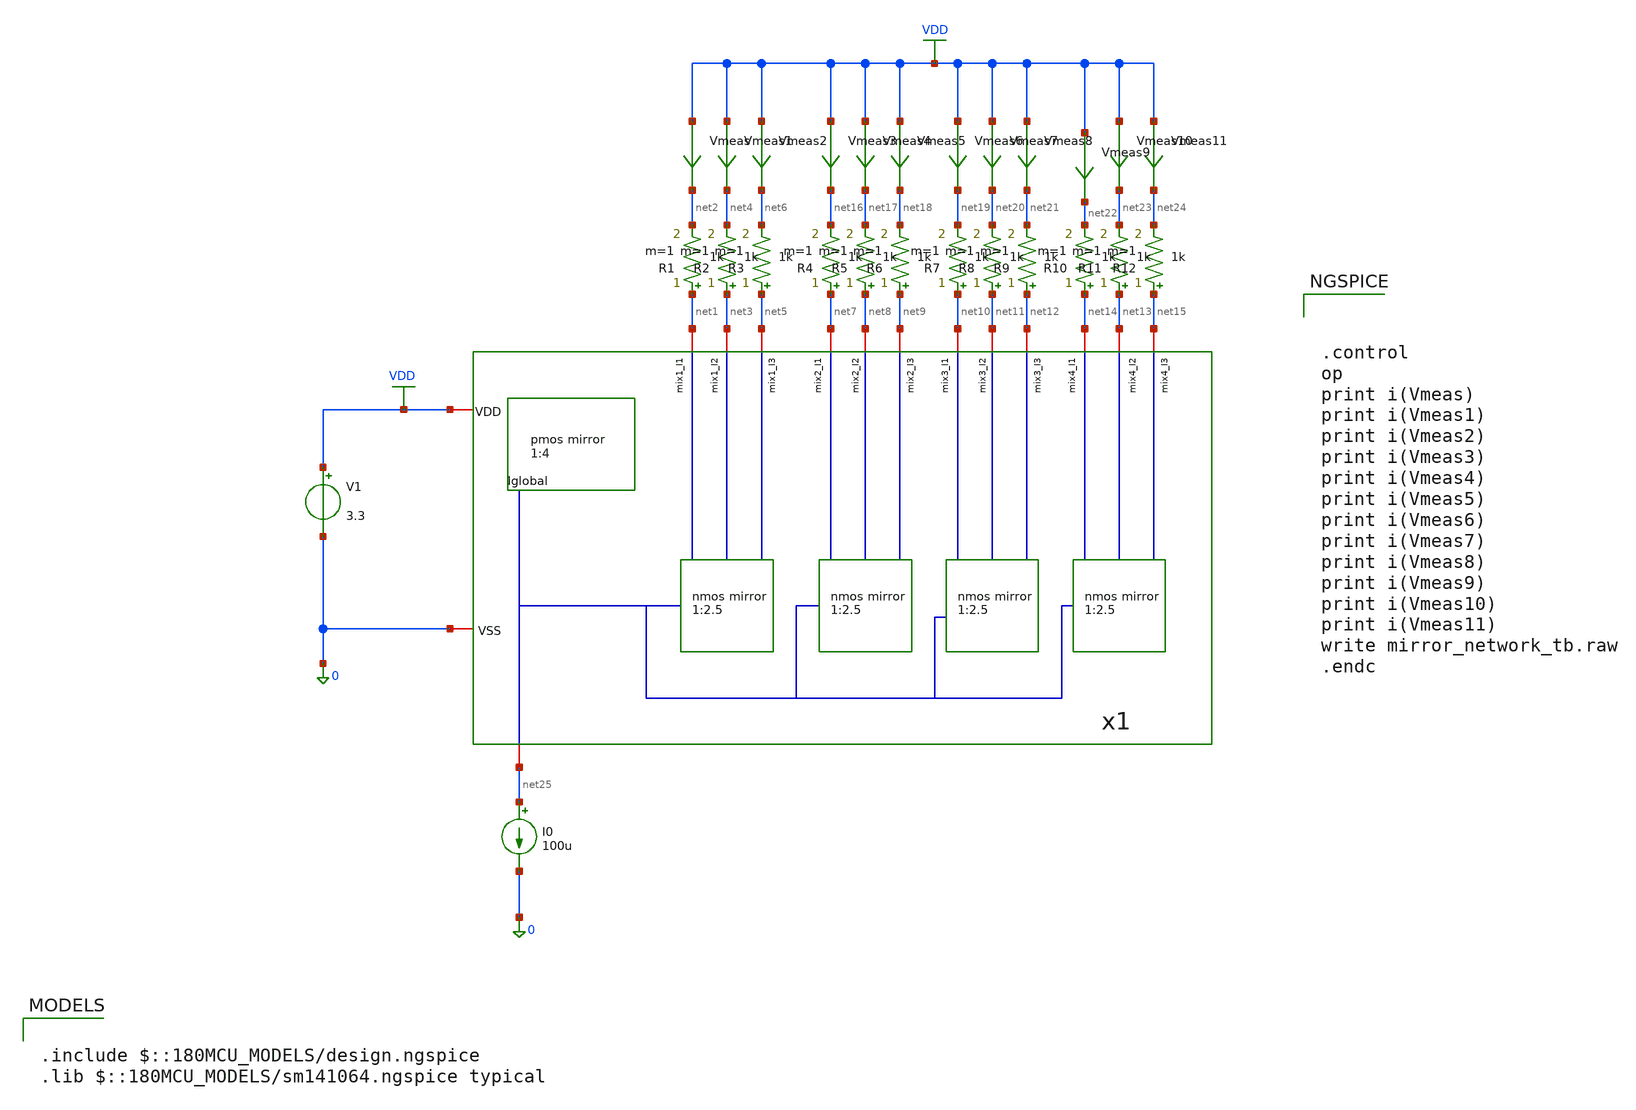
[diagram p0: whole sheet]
** sch_path: designs/mirrors/testbench/mirror_network_tb.sch
**.subckt mirror_network_tb
x1 VDD net25 net14 net1 net13 net15 net3 net5 0 net10 net11 net12 net7 net8 net9 mirror_network
V1 VDD 0 3.3
I0 net25 0 100u
R1 net1 net2 1k m=1
R2 net3 net4 1k m=1
R3 net5 net6 1k m=1
R4 net7 net16 1k m=1
R5 net8 net17 1k m=1
R6 net9 net18 1k m=1
R7 net10 net19 1k m=1
R8 net11 net20 1k m=1
R9 net12 net21 1k m=1
R10 net14 net22 1k m=1
R11 net13 net23 1k m=1
R12 net15 net24 1k m=1
Vmeas VDD net2 0
.save i(vmeas)
Vmeas1 VDD net4 0
.save i(vmeas1)
Vmeas2 VDD net6 0
.save i(vmeas2)
Vmeas3 VDD net16 0
.save i(vmeas3)
Vmeas4 VDD net17 0
.save i(vmeas4)
Vmeas5 VDD net18 0
.save i(vmeas5)
Vmeas6 VDD net19 0
.save i(vmeas6)
Vmeas7 VDD net20 0
.save i(vmeas7)
Vmeas8 VDD net21 0
.save i(vmeas8)
Vmeas9 VDD net22 0
.save i(vmeas9)
Vmeas10 VDD net23 0
.save i(vmeas10)
Vmeas11 VDD net24 0
.save i(vmeas11)
**** begin user architecture code

.include $::180MCU_MODELS/design.ngspice
.lib $::180MCU_MODELS/sm141064.ngspice typical




.control
op
print i(Vmeas)
print i(Vmeas1)
print i(Vmeas2)
print i(Vmeas3)
print i(Vmeas4)
print i(Vmeas5)
print i(Vmeas6)
print i(Vmeas7)
print i(Vmeas8)
print i(Vmeas9)
print i(Vmeas10)
print i(Vmeas11)
write mirror_network_tb.raw
.endc


**** end user architecture code
**.ends

* expanding   symbol:  /foss/designs/NYCMOS/designs/mirrors/schematic/mirror_network.sym # of
*+ pins=15
** sym_path: designs/mirrors/schematic/mirror_network.sym
** sch_path: designs/mirrors/schematic/mirror_network.sch
.subckt mirror_network VDD Iglobal mix4_I1 mix1_I1 mix4_I2 mix4_I3 mix1_I2 mix1_I3 VSS mix3_I1
+ mix3_I2 mix3_I3 mix2_I1 mix2_I2 mix2_I3
*.iopin VSS
*.iopin VDD
*.iopin Iglobal
*.iopin mix1_I1
*.iopin mix1_I2
*.iopin mix1_I3
*.iopin mix2_I1
*.iopin mix2_I2
*.iopin mix2_I3
*.iopin mix3_I1
*.iopin mix3_I2
*.iopin mix3_I3
*.iopin mix4_I1
*.iopin mix4_I2
*.iopin mix4_I3
x1 VDD net1 Iglobal pmos_mirror
x2 net1 mix1_I1 mix1_I2 mix1_I3 VSS nmos_mirror
x3 net1 mix2_I1 mix2_I2 mix2_I3 VSS nmos_mirror
x4 net1 mix3_I1 mix3_I2 mix3_I3 VSS nmos_mirror
x5 net1 mix4_I1 mix4_I2 mix4_I3 VSS nmos_mirror
.ends


* expanding   symbol:  /foss/designs/NYCMOS/designs/mirrors/schematic/pmos_mirror.sym # of pins=3
** sym_path: designs/mirrors/schematic/pmos_mirror.sym
** sch_path: designs/mirrors/schematic/pmos_mirror.sch
.subckt pmos_mirror VDD Iout Iref
*.iopin Iref
*.iopin Iout
*.iopin VDD
XM1 Iref Iref VDD VDD pfet_03v3 L=0.5u W=28u nf=7 ad='int((nf+1)/2) * W/nf * 0.18u' as='int((nf+2)/2) * W/nf * 0.18u'
+ pd='2*int((nf+1)/2) * (W/nf + 0.18u)' ps='2*int((nf+2)/2) * (W/nf + 0.18u)' nrd='0.18u / W' nrs='0.18u / W'
+ sa=0 sb=0 sd=0 m=1
XM2 Iout Iref VDD VDD pfet_03v3 L=0.5u W=28u nf=7 ad='int((nf+1)/2) * W/nf * 0.18u' as='int((nf+2)/2) * W/nf * 0.18u'
+ pd='2*int((nf+1)/2) * (W/nf + 0.18u)' ps='2*int((nf+2)/2) * (W/nf + 0.18u)' nrd='0.18u / W' nrs='0.18u / W'
+ sa=0 sb=0 sd=0 m=1
.ends


* expanding   symbol:  /foss/designs/NYCMOS/designs/mirrors/schematic/nmos_mirror.sym # of pins=5
** sym_path: designs/mirrors/schematic/nmos_mirror.sym
** sch_path: designs/mirrors/schematic/nmos_mirror.sch
.subckt nmos_mirror Ilocal I1_250u I2_250u I3_250u VSS
*.iopin VSS
*.iopin Ilocal
*.iopin I1_250u
*.iopin I2_250u
*.iopin I3_250u
XM1 Ilocal Ilocal VSS VSS nfet_03v3 L=0.5u W=8u nf=2 ad='int((nf+1)/2) * W/nf * 0.18u' as='int((nf+2)/2) * W/nf * 0.18u'
+ pd='2*int((nf+1)/2) * (W/nf + 0.18u)' ps='2*int((nf+2)/2) * (W/nf + 0.18u)' nrd='0.18u / W' nrs='0.18u / W'
+ sa=0 sb=0 sd=0 m=1
XM2 I1_250u Ilocal VSS VSS nfet_03v3 L=0.5u W=20u nf=5 ad='int((nf+1)/2) * W/nf * 0.18u' as='int((nf+2)/2) * W/nf * 0.18u'
+ pd='2*int((nf+1)/2) * (W/nf + 0.18u)' ps='2*int((nf+2)/2) * (W/nf + 0.18u)' nrd='0.18u / W' nrs='0.18u / W'
+ sa=0 sb=0 sd=0 m=1
XM3 I2_250u Ilocal VSS VSS nfet_03v3 L=0.5u W=20u nf=5 ad='int((nf+1)/2) * W/nf * 0.18u' as='int((nf+2)/2) * W/nf * 0.18u'
+ pd='2*int((nf+1)/2) * (W/nf + 0.18u)' ps='2*int((nf+2)/2) * (W/nf + 0.18u)' nrd='0.18u / W' nrs='0.18u / W'
+ sa=0 sb=0 sd=0 m=1
XM4 I3_250u Ilocal VSS VSS nfet_03v3 L=0.5u W=20u nf=5 ad='int((nf+1)/2) * W/nf * 0.18u' as='int((nf+2)/2) * W/nf * 0.18u'
+ pd='2*int((nf+1)/2) * (W/nf + 0.18u)' ps='2*int((nf+2)/2) * (W/nf + 0.18u)' nrd='0.18u / W' nrs='0.18u / W'
+ sa=0 sb=0 sd=0 m=1
.ends

.GLOBAL VDD
.end
